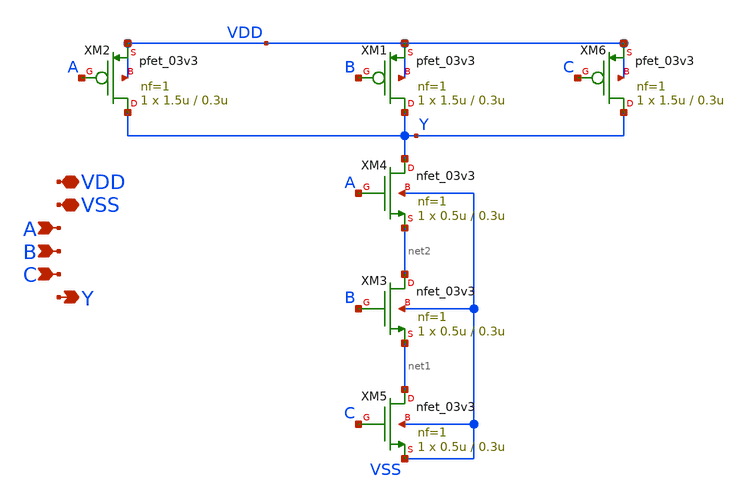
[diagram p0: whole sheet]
** sch_path: designs/libs/core_analog/switch-matrix/nand3_1.sch
**.subckt nand3_1 VDD VSS A B Y C
*.iopin VDD
*.iopin VSS
*.ipin A
*.ipin B
*.opin Y
*.ipin C
XM2 Y A VDD VDD pfet_03v3 L=0.3u W=1.5u nf=1 ad='int((nf+1)/2) * W/nf * 0.18u' as='int((nf+2)/2) * W/nf * 0.18u'
+ pd='2*int((nf+1)/2) * (W/nf + 0.18u)' ps='2*int((nf+2)/2) * (W/nf + 0.18u)' nrd='0.18u / W' nrs='0.18u / W'
+ sa=0 sb=0 sd=0 m=1
XM1 Y B VDD VDD pfet_03v3 L=0.3u W=1.5u nf=1 ad='int((nf+1)/2) * W/nf * 0.18u' as='int((nf+2)/2) * W/nf * 0.18u'
+ pd='2*int((nf+1)/2) * (W/nf + 0.18u)' ps='2*int((nf+2)/2) * (W/nf + 0.18u)' nrd='0.18u / W' nrs='0.18u / W'
+ sa=0 sb=0 sd=0 m=1
XM6 Y C VDD VDD pfet_03v3 L=0.3u W=1.5u nf=1 ad='int((nf+1)/2) * W/nf * 0.18u' as='int((nf+2)/2) * W/nf * 0.18u'
+ pd='2*int((nf+1)/2) * (W/nf + 0.18u)' ps='2*int((nf+2)/2) * (W/nf + 0.18u)' nrd='0.18u / W' nrs='0.18u / W'
+ sa=0 sb=0 sd=0 m=1
XM4 Y A net2 VSS nfet_03v3 L=0.3u W=0.5u nf=1 ad='int((nf+1)/2) * W/nf * 0.18u' as='int((nf+2)/2) * W/nf * 0.18u'
+ pd='2*int((nf+1)/2) * (W/nf + 0.18u)' ps='2*int((nf+2)/2) * (W/nf + 0.18u)' nrd='0.18u / W' nrs='0.18u / W'
+ sa=0 sb=0 sd=0 m=1
XM3 net2 B net1 VSS nfet_03v3 L=0.3u W=0.5u nf=1 ad='int((nf+1)/2) * W/nf * 0.18u' as='int((nf+2)/2) * W/nf * 0.18u'
+ pd='2*int((nf+1)/2) * (W/nf + 0.18u)' ps='2*int((nf+2)/2) * (W/nf + 0.18u)' nrd='0.18u / W' nrs='0.18u / W'
+ sa=0 sb=0 sd=0 m=1
XM5 net1 C VSS VSS nfet_03v3 L=0.3u W=0.5u nf=1 ad='int((nf+1)/2) * W/nf * 0.18u' as='int((nf+2)/2) * W/nf * 0.18u'
+ pd='2*int((nf+1)/2) * (W/nf + 0.18u)' ps='2*int((nf+2)/2) * (W/nf + 0.18u)' nrd='0.18u / W' nrs='0.18u / W'
+ sa=0 sb=0 sd=0 m=1
**.ends
.end
